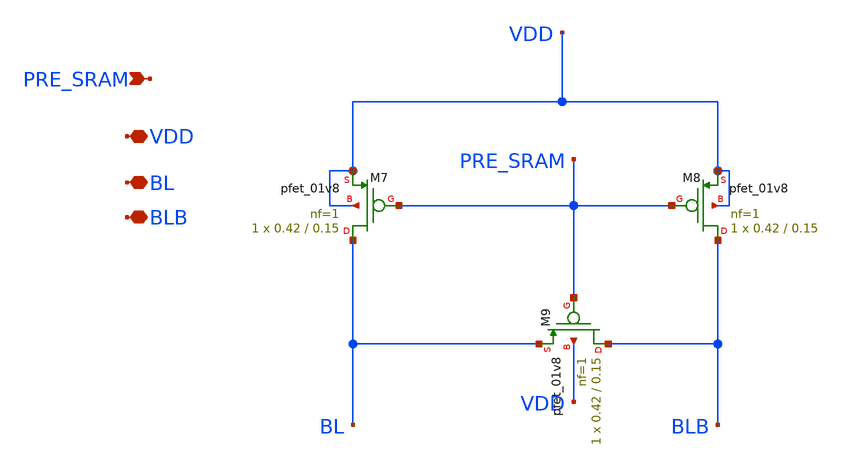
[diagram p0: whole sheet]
** sch_path: xschem/Integrated_bitcell/Precharge.sch
**.subckt Precharge PRE_SRAM VDD BL BLB
*.ipin PRE_SRAM
*.iopin VDD
*.iopin BL
*.iopin BLB
XM7 BL PRE_SRAM VDD VDD sky130_fd_pr__pfet_01v8 L=0.15 W=0.42 nf=1 ad='int((nf+1)/2) * W/nf * 0.29' as='int((nf+2)/2) * W/nf * 0.29'
+ pd='2*int((nf+1)/2) * (W/nf + 0.29)' ps='2*int((nf+2)/2) * (W/nf + 0.29)' nrd='0.29 / W' nrs='0.29 / W'
+ sa=0 sb=0 sd=0 mult=1 m=1
XM8 BLB PRE_SRAM VDD VDD sky130_fd_pr__pfet_01v8 L=0.15 W=0.42 nf=1 ad='int((nf+1)/2) * W/nf * 0.29'
+ as='int((nf+2)/2) * W/nf * 0.29' pd='2*int((nf+1)/2) * (W/nf + 0.29)' ps='2*int((nf+2)/2) * (W/nf + 0.29)'
+ nrd='0.29 / W' nrs='0.29 / W' sa=0 sb=0 sd=0 mult=1 m=1
XM9 BLB PRE_SRAM BL VDD sky130_fd_pr__pfet_01v8 L=0.15 W=0.42 nf=1 ad='int((nf+1)/2) * W/nf * 0.29' as='int((nf+2)/2) * W/nf * 0.29'
+ pd='2*int((nf+1)/2) * (W/nf + 0.29)' ps='2*int((nf+2)/2) * (W/nf + 0.29)' nrd='0.29 / W' nrs='0.29 / W'
+ sa=0 sb=0 sd=0 mult=1 m=1
**.ends
.end
